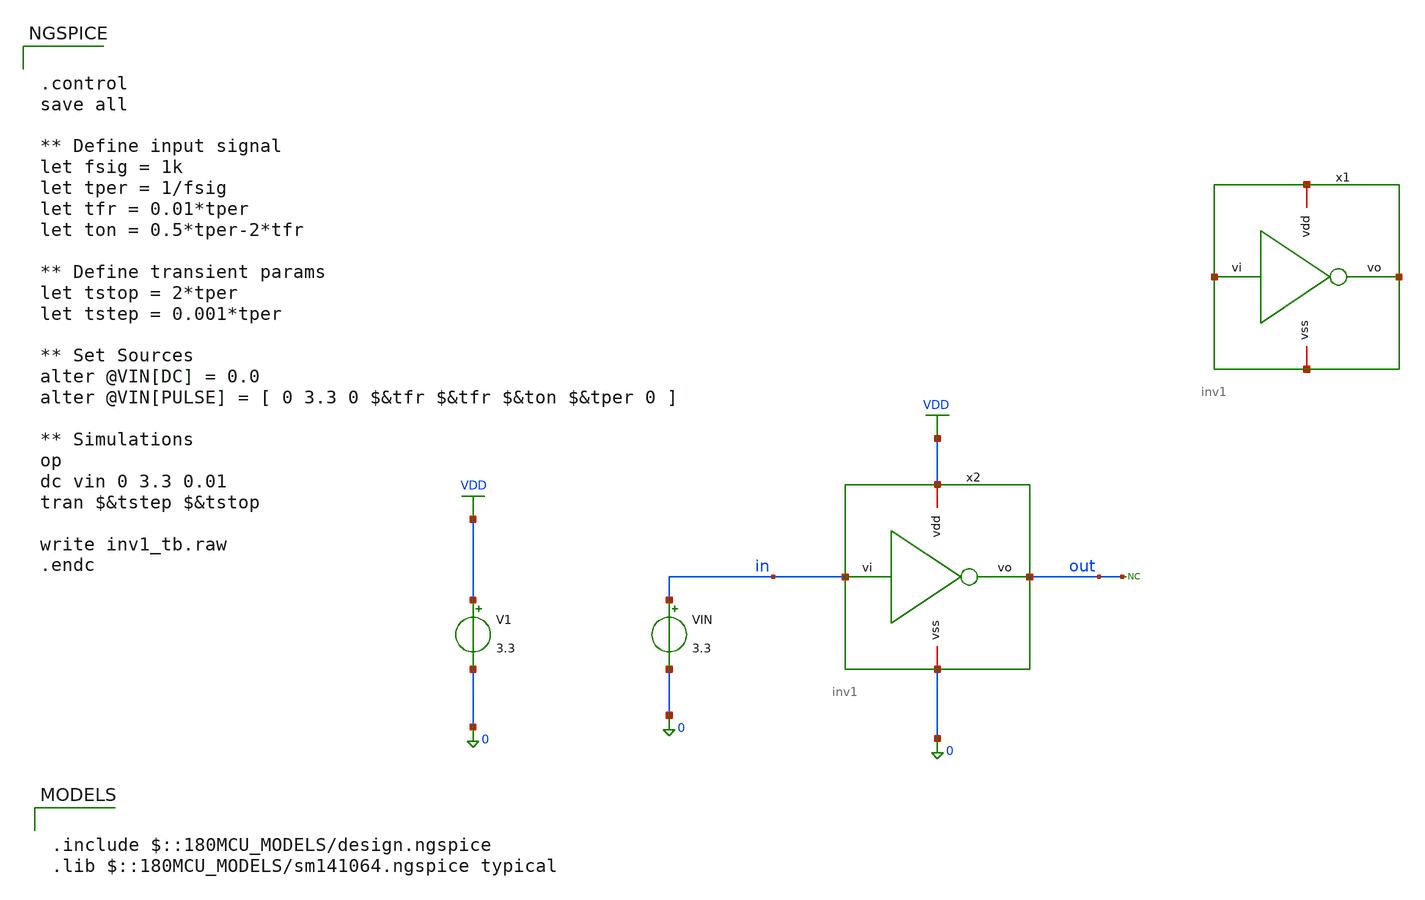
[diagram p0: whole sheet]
** sch_path: comparator/schematic/inv1_tb.sch
**.subckt inv1_tb
x1 net1 net2 net3 net4 inv1
V1 VDD 0 3.3
VIN in 0 3.3
* noconn out
x2 VDD in out 0 inv1
**** begin user architecture code

.include $::180MCU_MODELS/design.ngspice
.lib $::180MCU_MODELS/sm141064.ngspice typical



.control
save all

** Define input signal
let fsig = 1k
let tper = 1/fsig
let tfr = 0.01*tper
let ton = 0.5*tper-2*tfr

** Define transient params
let tstop = 2*tper
let tstep = 0.001*tper

** Set Sources
alter @VIN[DC] = 0.0
alter @VIN[PULSE] = [ 0 3.3 0 $&tfr $&tfr $&ton $&tper 0 ]

** Simulations
op
dc vin 0 3.3 0.01
tran $&tstep $&tstop

write inv1_tb.raw
.endc


**** end user architecture code
**.ends
.GLOBAL VDD
.end
